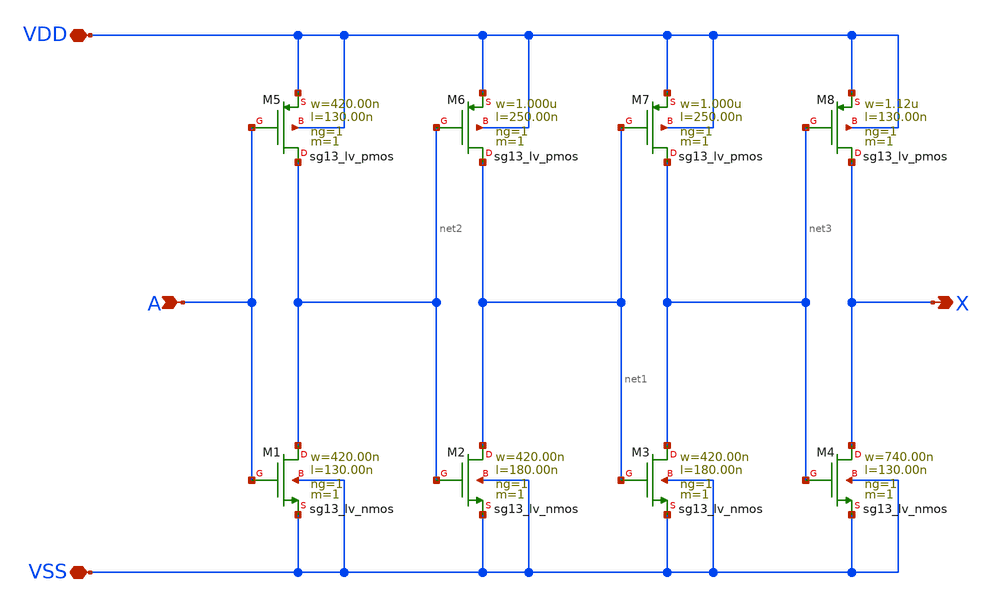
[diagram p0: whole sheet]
** sch_path: ihp-sg13g2/libs.tech/xschem/sg13g2_stdcells/sg13g2_dlygate4sd2_1.sch
**.subckt sg13g2_dlygate4sd2_1 A X VDD VSS
*.ipin A
*.opin X
*.iopin VDD
*.iopin VSS
XM1 net2 A VSS VSS sg13_lv_nmos w=420.00n l=130.00n ng=1 m=1 mm_ok=1
XM2 net1 net2 VSS VSS sg13_lv_nmos w=420.00n l=180.00n ng=1 m=1 mm_ok=1
XM3 net3 net1 VSS VSS sg13_lv_nmos w=420.00n l=180.00n ng=1 m=1 mm_ok=1
XM4 X net3 VSS VSS sg13_lv_nmos w=740.00n l=130.00n ng=1 m=1 mm_ok=1
XM5 net2 A VDD VDD sg13_lv_pmos w=420.00n l=130.00n ng=1 m=1 mm_ok=1
XM6 net1 net2 VDD VDD sg13_lv_pmos w=1.000u l=250.00n ng=1 m=1 mm_ok=1
XM7 net3 net1 VDD VDD sg13_lv_pmos w=1.000u l=250.00n ng=1 m=1 mm_ok=1
XM8 X net3 VDD VDD sg13_lv_pmos w=1.12u l=130.00n ng=1 m=1 mm_ok=1
**.ends
.end
